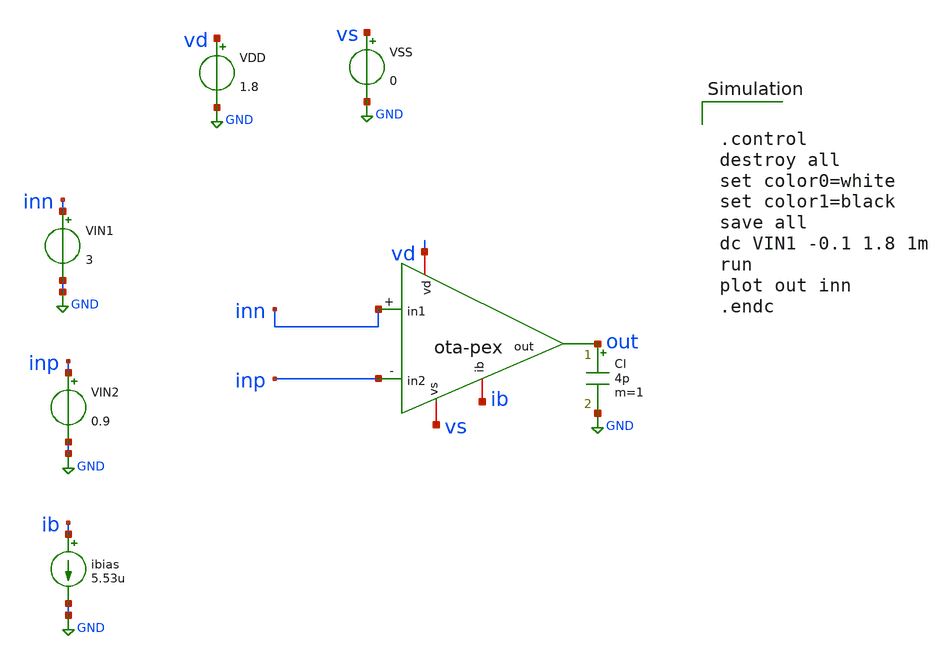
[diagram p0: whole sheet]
** sch_path: ota/xschem/ota_tb-dc.sch
* Copyright 2020 Stefan Frederik Schippers
* Licensed under the Apache License, Version 2.0 (the "License");
* you may not use this file except in compliance with the License.
* You may obtain a copy of the License at
* https://www.apache.org/licenses/LICENSE-2.0
* Unless required by applicable law or agreed to in writing, software
* distributed under the License is distributed on an "AS IS" BASIS,
* WITHOUT WARRANTIES OR CONDITIONS OF ANY KIND, either express or implied.
* See the License for the specific language governing permissions and
* limitations under the License.
**.subckt ota_tb-dc
VIN1 inn GND 3
ibias ib GND 5.53u
VDD vd GND 1.8
VSS vs GND 0
Cl out GND 4p m=1
VIN2 inp GND 0.9
X1 vd ib out inp inn vs ota-pex
**** begin user architecture code


.control
destroy all
set color0=white
set color1=black
save all
dc VIN1 -0.1 1.8 1m
run
plot out inn
.endc

 .lib $::SKYWATER_MODELS/sky130.lib.spice tt
.include $::SKYWATER_STDCELLS/sky130_fd_sc_hd.spice

**** end user architecture code
**.ends
.GLOBAL GND
.end
